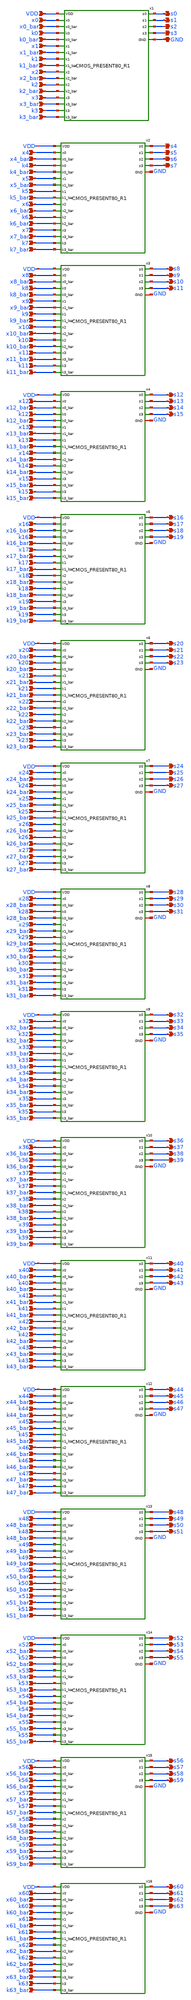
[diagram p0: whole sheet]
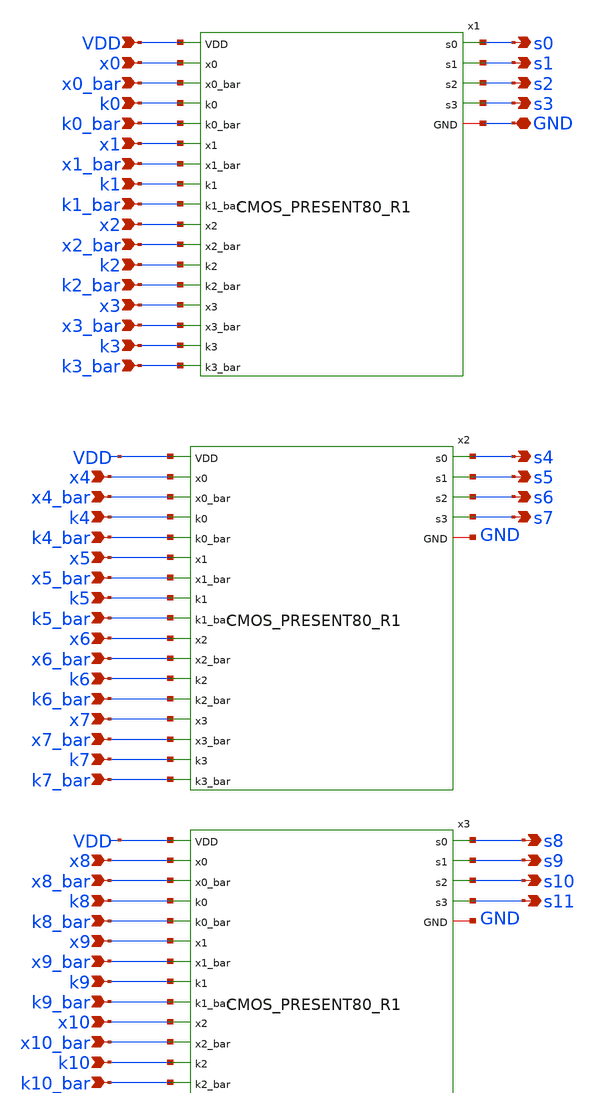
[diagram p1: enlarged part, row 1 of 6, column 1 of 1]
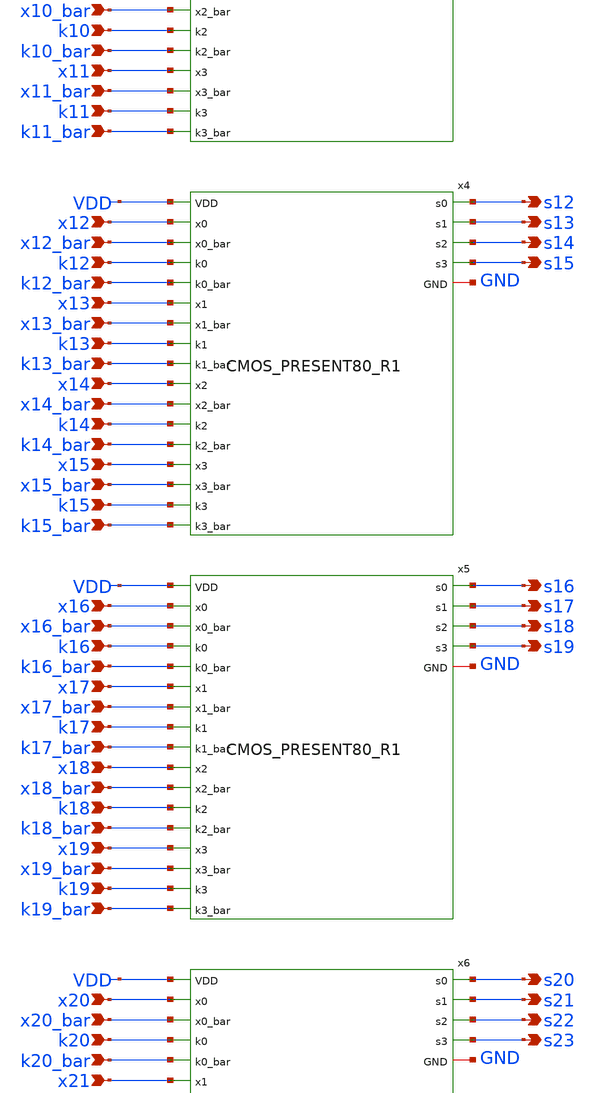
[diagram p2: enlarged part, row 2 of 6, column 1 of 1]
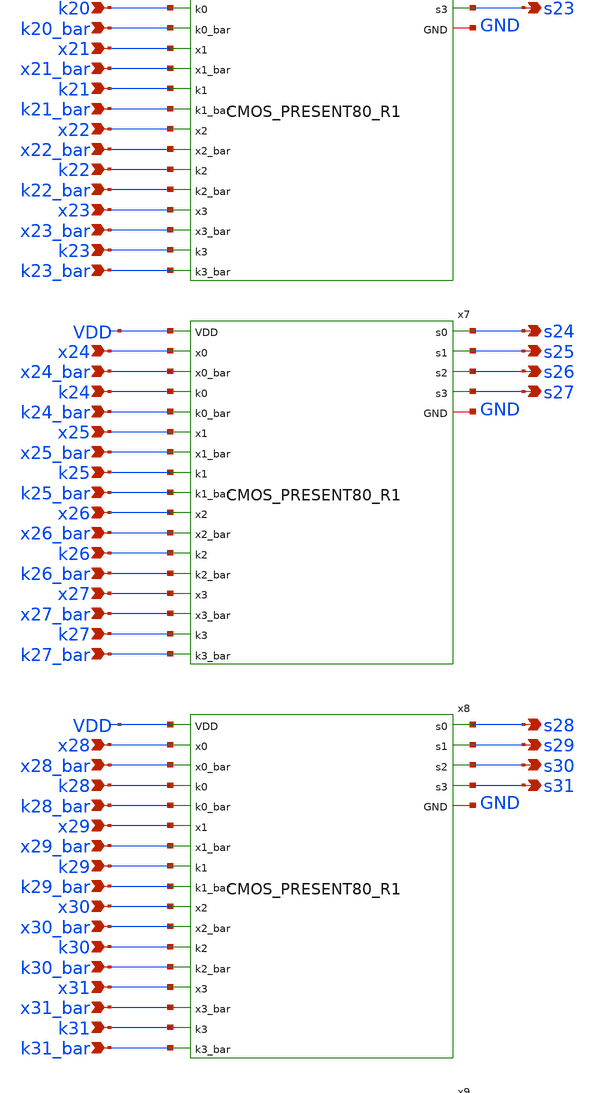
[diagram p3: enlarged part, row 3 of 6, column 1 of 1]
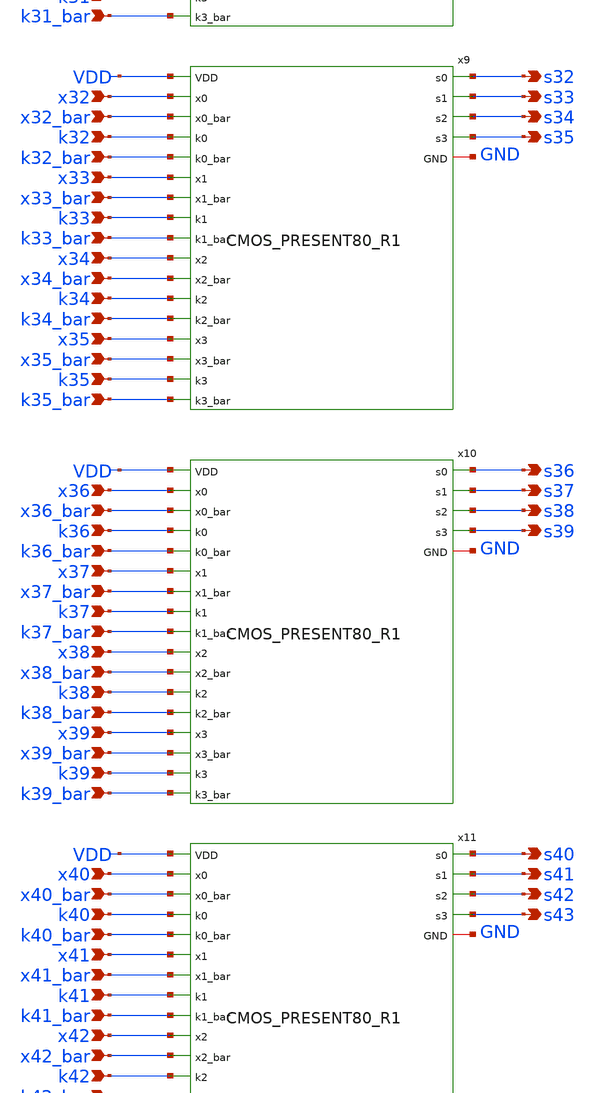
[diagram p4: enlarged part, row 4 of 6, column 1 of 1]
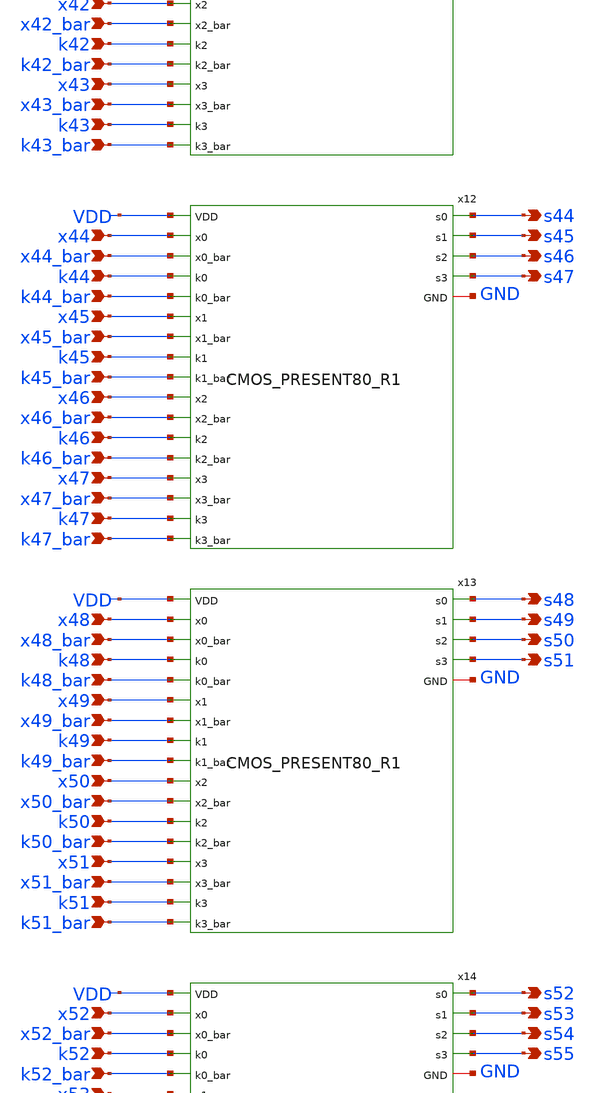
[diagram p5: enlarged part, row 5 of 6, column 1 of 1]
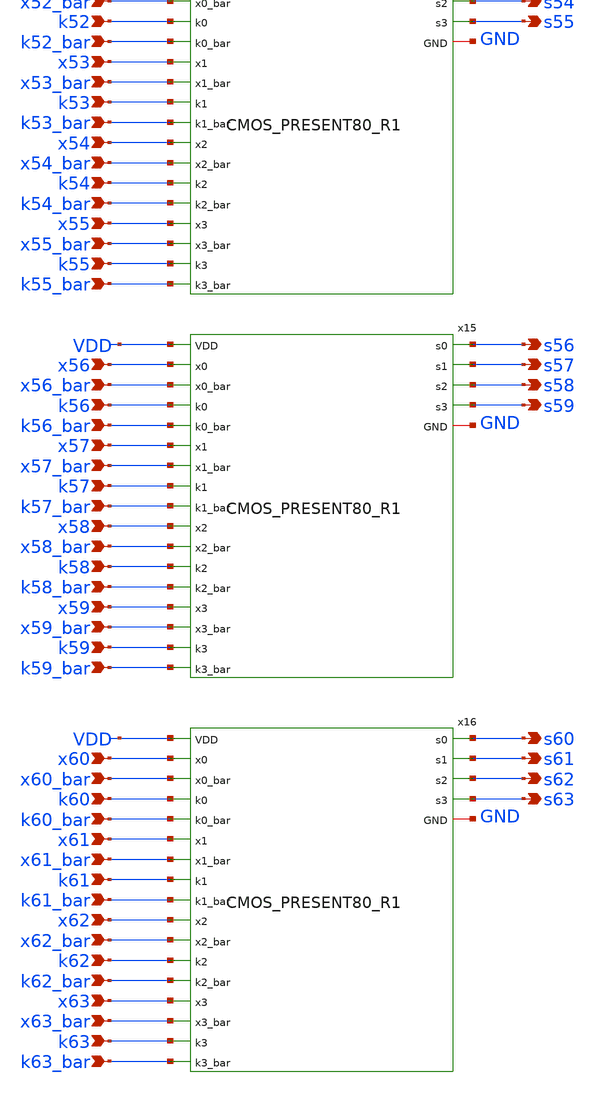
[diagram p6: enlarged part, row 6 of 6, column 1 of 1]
** sch_path: skywater_stuff/CMOS_64bitwidth_PRESENT80_R1Test.sch
**.subckt CMOS_64bitwidth_PRESENT80_R1Test x0 x0_bar k0 k0_bar x1 x1_bar k1 k1_bar x2 x2_bar k2
*+ k2_bar x3 x3_bar k3 k3_bar x4 x4_bar k4 k4_bar x5 x5_bar k5 k5_bar x6 x6_bar k6 k6_bar x7 x7_bar k7 k7_bar
*+ x8 x8_bar k8 k8_bar x9 x9_bar k9 k9_bar x10 x10_bar k10 k10_bar x11 x11_bar k11_bar k11 x12 x12_bar
*+ k12_bar k12 x13 x13_bar k13 k13_bar x14 x14_bar k14 k14_bar x15 x15_bar k15 k15_bar x16 x16_bar k16 k16_bar
*+ x17 x17_bar k17 k17_bar x18 x18_bar k18 k18_bar x19 x19_bar k19 k19_bar x20 x20_bar k20 k20_bar x21
*+ x21_bar k21 k21_bar x22 x22_bar k22 k22_bar x23 x23_bar k23 k23_bar x24 x24_bar k24 k24_bar x25 x25_bar k25
*+ k25_bar x26 x26_bar k26 k26_bar x27 x27_bar k27 k27_bar x28 x28_bar k28 k28_bar x29 x29_bar k29 k29_bar x30
*+ x30_bar k30 k30_bar x31 x31_bar k31 k31_bar x32 x32_bar k32 k32_bar x33 x33_bar k33 k33_bar x34 x34_bar k34
*+ k34_bar x35 x35_bar k35 k35_bar x36 x36_bar k36 k36_bar x37 x37_bar k37 k37_bar x38 x38_bar k38 k38_bar x39
*+ x39_bar k39 k39_bar x40 x40_bar k40 k40_bar x41 x41_bar k41 k41_bar x42 x42_bar k42 k42_bar x43 x43_bar k43
*+ k43_bar x44 x44_bar k44 k44_bar x45 x45_bar k45 k45_bar x46 x46_bar k46 k46_bar x47 x47_bar k47 k47_bar x48
*+ x48_bar k48 k48_bar x49 x49_bar k49 k49_bar x50 x50_bar k50 k50_bar x51 x51_bar k51 k51_bar x52 x52_bar k52
*+ k52_bar x53 x53_bar k53 k53_bar x54 x54_bar k54 k54_bar x55 x55_bar k55 k55_bar x56 x56_bar k56 k56_bar x57
*+ x57_bar k57 k57_bar x58 x58_bar k58 k58_bar x59 x59_bar k59 k59_bar x60 x60_bar k60 k60_bar x61 x61_bar k61
*+ k61_bar x62 x62_bar k62 k62_bar x63 x63_bar k63 k63_bar s0 s1 s2 s3 s4 s5 s6 s7 s8 s9 s10 s11 s12 s13 s14
*+ s15 s16 s17 s18 s19 s20 s21 s22 s23 s24 s25 s26 s27 s28 s29 s30 s31 s32 s33 s34 s35 s36 s37 s38 s39 s40
*+ s41 s42 s43 s44 s45 s46 s47 s48 s49 s50 s51 s52 s53 s54 s55 s56 s57 s58 s59 s60 s61 s62 s63 GND VDD
*.ipin x0
*.ipin x0_bar
*.ipin k0
*.ipin k0_bar
*.ipin x1
*.ipin x1_bar
*.ipin k1
*.ipin k1_bar
*.ipin x2
*.ipin x2_bar
*.ipin k2
*.ipin k2_bar
*.ipin x3
*.ipin x3_bar
*.ipin k3
*.ipin k3_bar
*.ipin x4
*.ipin x4_bar
*.ipin k4
*.ipin k4_bar
*.ipin x5
*.ipin x5_bar
*.ipin k5
*.ipin k5_bar
*.ipin x6
*.ipin x6_bar
*.ipin k6
*.ipin k6_bar
*.ipin x7
*.ipin x7_bar
*.ipin k7
*.ipin k7_bar
*.ipin x8
*.ipin x8_bar
*.ipin k8
*.ipin k8_bar
*.ipin x9
*.ipin x9_bar
*.ipin k9
*.ipin k9_bar
*.ipin x10
*.ipin x10_bar
*.ipin k10
*.ipin k10_bar
*.ipin x11
*.ipin x11_bar
*.ipin k11_bar
*.ipin k11
*.ipin x12
*.ipin x12_bar
*.ipin k12_bar
*.ipin k12
*.ipin x13
*.ipin x13_bar
*.ipin k13
*.ipin k13_bar
*.ipin x14
*.ipin x14_bar
*.ipin k14
*.ipin k14_bar
*.ipin x15
*.ipin x15_bar
*.ipin k15
*.ipin k15_bar
*.ipin x16
*.ipin x16_bar
*.ipin k16
*.ipin k16_bar
*.ipin x17
*.ipin x17_bar
*.ipin k17
*.ipin k17_bar
*.ipin x18
*.ipin x18_bar
*.ipin k18
*.ipin k18_bar
*.ipin x19
*.ipin x19_bar
*.ipin k19
*.ipin k19_bar
*.ipin x20
*.ipin x20_bar
*.ipin k20
*.ipin k20_bar
*.ipin x21
*.ipin x21_bar
*.ipin k21
*.ipin k21_bar
*.ipin x22
*.ipin x22_bar
*.ipin k22
*.ipin k22_bar
*.ipin x23
*.ipin x23_bar
*.ipin k23
*.ipin k23_bar
*.ipin x24
*.ipin x24_bar
*.ipin k24
*.ipin k24_bar
*.ipin x25
*.ipin x25_bar
*.ipin k25
*.ipin k25_bar
*.ipin x26
*.ipin x26_bar
*.ipin k26
*.ipin k26_bar
*.ipin x27
*.ipin x27_bar
*.ipin k27
*.ipin k27_bar
*.ipin x28
*.ipin x28_bar
*.ipin k28
*.ipin k28_bar
*.ipin x29
*.ipin x29_bar
*.ipin k29
*.ipin k29_bar
*.ipin x30
*.ipin x30_bar
*.ipin k30
*.ipin k30_bar
*.ipin x31
*.ipin x31_bar
*.ipin k31
*.ipin k31_bar
*.ipin x32
*.ipin x32_bar
*.ipin k32
*.ipin k32_bar
*.ipin x33
*.ipin x33_bar
*.ipin k33
*.ipin k33_bar
*.ipin x34
*.ipin x34_bar
*.ipin k34
*.ipin k34_bar
*.ipin x35
*.ipin x35_bar
*.ipin k35
*.ipin k35_bar
*.ipin x36
*.ipin x36_bar
*.ipin k36
*.ipin k36_bar
*.ipin x37
*.ipin x37_bar
*.ipin k37
*.ipin k37_bar
*.ipin x38
*.ipin x38_bar
*.ipin k38
*.ipin k38_bar
*.ipin x39
*.ipin x39_bar
*.ipin k39
*.ipin k39_bar
*.ipin x40
*.ipin x40_bar
*.ipin k40
*.ipin k40_bar
*.ipin x41
*.ipin x41_bar
*.ipin k41
*.ipin k41_bar
*.ipin x42
*.ipin x42_bar
*.ipin k42
*.ipin k42_bar
*.ipin x43
*.ipin x43_bar
*.ipin k43
*.ipin k43_bar
*.ipin x44
*.ipin x44_bar
*.ipin k44
*.ipin k44_bar
*.ipin x45
*.ipin x45_bar
*.ipin k45
*.ipin k45_bar
*.ipin x46
*.ipin x46_bar
*.ipin k46
*.ipin k46_bar
*.ipin x47
*.ipin x47_bar
*.ipin k47
*.ipin k47_bar
*.ipin x48
*.ipin x48_bar
*.ipin k48
*.ipin k48_bar
*.ipin x49
*.ipin x49_bar
*.ipin k49
*.ipin k49_bar
*.ipin x50
*.ipin x50_bar
*.ipin k50
*.ipin k50_bar
*.ipin x51
*.ipin x51_bar
*.ipin k51
*.ipin k51_bar
*.ipin x52
*.ipin x52_bar
*.ipin k52
*.ipin k52_bar
*.ipin x53
*.ipin x53_bar
*.ipin k53
*.ipin k53_bar
*.ipin x54
*.ipin x54_bar
*.ipin k54
*.ipin k54_bar
*.ipin x55
*.ipin x55_bar
*.ipin k55
*.ipin k55_bar
*.ipin x56
*.ipin x56_bar
*.ipin k56
*.ipin k56_bar
*.ipin x57
*.ipin x57_bar
*.ipin k57
*.ipin k57_bar
*.ipin x58
*.ipin x58_bar
*.ipin k58
*.ipin k58_bar
*.ipin x59
*.ipin x59_bar
*.ipin k59
*.ipin k59_bar
*.ipin x60
*.ipin x60_bar
*.ipin k60
*.ipin k60_bar
*.ipin x61
*.ipin x61_bar
*.ipin k61
*.ipin k61_bar
*.ipin x62
*.ipin x62_bar
*.ipin k62
*.ipin k62_bar
*.ipin x63
*.ipin x63_bar
*.ipin k63
*.ipin k63_bar
*.opin s0
*.opin s1
*.opin s2
*.opin s3
*.opin s4
*.opin s5
*.opin s6
*.opin s7
*.opin s8
*.opin s9
*.opin s10
*.opin s11
*.opin s12
*.opin s13
*.opin s14
*.opin s15
*.opin s16
*.opin s17
*.opin s18
*.opin s19
*.opin s20
*.opin s21
*.opin s22
*.opin s23
*.opin s24
*.opin s25
*.opin s26
*.opin s27
*.opin s28
*.opin s29
*.opin s30
*.opin s31
*.opin s32
*.opin s33
*.opin s34
*.opin s35
*.opin s36
*.opin s37
*.opin s38
*.opin s39
*.opin s40
*.opin s41
*.opin s42
*.opin s43
*.opin s44
*.opin s45
*.opin s46
*.opin s47
*.opin s48
*.opin s49
*.opin s50
*.opin s51
*.opin s52
*.opin s53
*.opin s54
*.opin s55
*.opin s56
*.opin s57
*.opin s58
*.opin s59
*.opin s60
*.opin s61
*.opin s62
*.opin s63
*.iopin GND
*.ipin VDD
x2 VDD GND k4 k4_bar x4 x4_bar x5_bar x5 k5_bar k5 k6 k6_bar x6 x6_bar x7_bar x7 k7_bar k7 s7 s6 s5
+ s4 CMOS_PRESENT80_R1
x3 VDD GND k8 k8_bar x8 x8_bar x9_bar x9 k9_bar k9 k10 k10_bar x10 x10_bar x11_bar x11 k11_bar k11
+ s11 s10 s9 s8 CMOS_PRESENT80_R1
x4 VDD GND k12 k12_bar x12 x12_bar x13_bar x13 k13_bar k13 k14 k14_bar x14 x14_bar x15_bar x15
+ k15_bar k15 s15 s14 s13 s12 CMOS_PRESENT80_R1
x5 VDD GND k16 k16_bar x16 x16_bar x17_bar x17 k17_bar k17 k18 k18_bar x18 x18_bar x19_bar x19
+ k19_bar k19 s19 s18 s17 s16 CMOS_PRESENT80_R1
x6 VDD GND k20 k20_bar x20 x20_bar x21_bar x21 k21_bar k21 k22 k22_bar x22 x22_bar x23_bar x23
+ k23_bar k23 s23 s22 s21 s20 CMOS_PRESENT80_R1
x7 VDD GND k24 k24_bar x24 x24_bar x25_bar x25 k25_bar k25 k26 k26_bar x26 x26_bar x27_bar x27
+ k27_bar k27 s27 s26 s25 s24 CMOS_PRESENT80_R1
x8 VDD GND k28 k28_bar x28 x28_bar x29_bar x29 k29_bar k29 k30 k30_bar x30 x30_bar x31_bar x31
+ k31_bar k31 s31 s30 s29 s28 CMOS_PRESENT80_R1
x9 VDD GND k32 k32_bar x32 x32_bar x33_bar x33 k33_bar k33 k34 k34_bar x34 x34_bar x35_bar x35
+ k35_bar k35 s35 s34 s33 s32 CMOS_PRESENT80_R1
x10 VDD GND k36 k36_bar x36 x36_bar x37_bar x37 k37_bar k37 k38 k38_bar x38 x38_bar x39_bar x39
+ k39_bar k39 s39 s38 s37 s36 CMOS_PRESENT80_R1
x11 VDD GND k40 k40_bar x40 x40_bar x41_bar x41 k41_bar k41 k42 k42_bar x42 x42_bar x43_bar x43
+ k43_bar k43 s43 s42 s41 s40 CMOS_PRESENT80_R1
x12 VDD GND k44 k44_bar x44 x44_bar x45_bar x45 k45_bar k45 k46 k46_bar x46 x46_bar x47_bar x47
+ k47_bar k47 s47 s46 s45 s44 CMOS_PRESENT80_R1
x13 VDD GND k48 k48_bar x48 x48_bar x49_bar x49 k49_bar k49 k50 k50_bar x50 x50_bar x51_bar x51
+ k51_bar k51 s51 s50 s49 s48 CMOS_PRESENT80_R1
x14 VDD GND k52 k52_bar x52 x52_bar x53_bar x53 k53_bar k53 k54 k54_bar x54 x54_bar x55_bar x55
+ k55_bar k55 s55 s54 s53 s52 CMOS_PRESENT80_R1
x15 VDD GND k56 k56_bar x56 x56_bar x57_bar x57 k57_bar k57 k58 k58_bar x58 x58_bar x59_bar x59
+ k59_bar k59 s59 s58 s57 s56 CMOS_PRESENT80_R1
x16 VDD GND k60 k60_bar x60 x60_bar x61_bar x61 k61_bar k61 k62 k62_bar x62 x62_bar x63_bar x63
+ k63_bar k63 s63 s62 s61 s60 CMOS_PRESENT80_R1
x1 VDD GND k0 k0_bar x0 x0_bar x1_bar x1 k1_bar k1 k2 k2_bar x2 x2_bar x3_bar x3 k3_bar k3 s3 s2 s1
+ s0 CMOS_PRESENT80_R1
**.ends
.end
